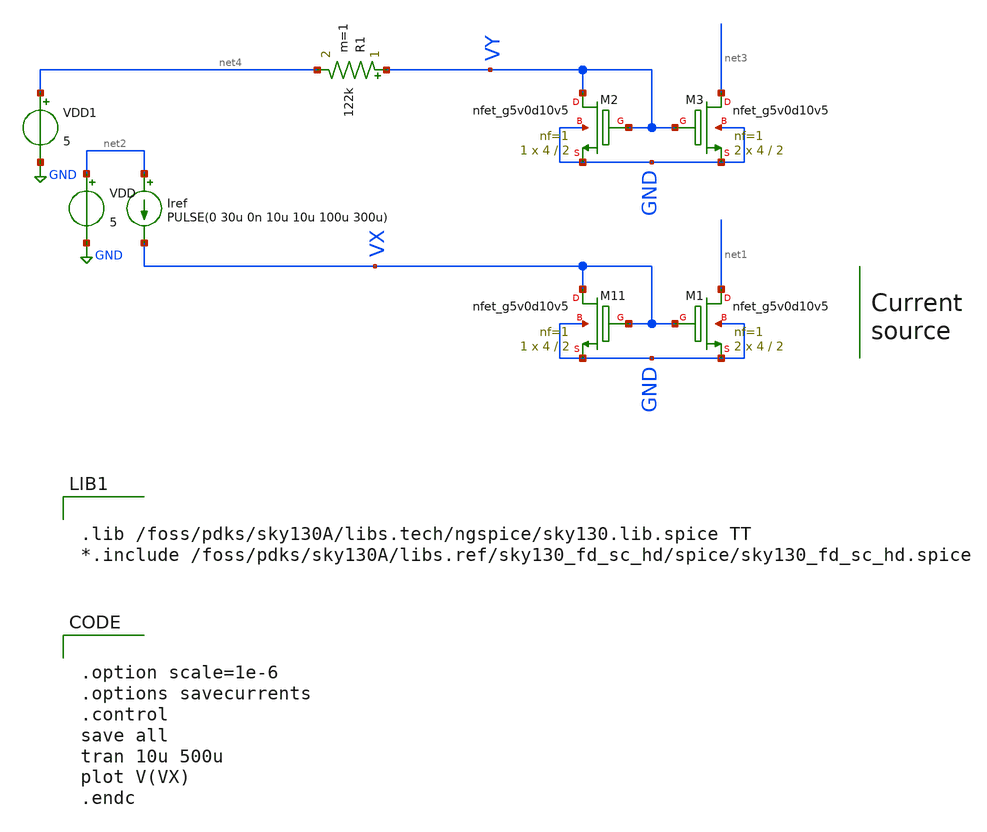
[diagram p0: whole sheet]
** sch_path: xschem/test/tb_current_source.sch
**.subckt tb_current_source
Iref net2 VX PULSE(0 30u 0n 10u 10u 100u 300u)
XM11 VX VX GND GND sky130_fd_pr__nfet_g5v0d10v5 L=2 W=4 nf=1 ad='int((nf+1)/2) * W/nf * 0.29' as='int((nf+2)/2) * W/nf * 0.29'
+ pd='2*int((nf+1)/2) * (W/nf + 0.29)' ps='2*int((nf+2)/2) * (W/nf + 0.29)' nrd='0.29 / W' nrs='0.29 / W'
+ sa=0 sb=0 sd=0 mult=1 m=1
XM1 net1 VX GND GND sky130_fd_pr__nfet_g5v0d10v5 L=2 W=4 nf=1 ad='int((nf+1)/2) * W/nf * 0.29' as='int((nf+2)/2) * W/nf * 0.29'
+ pd='2*int((nf+1)/2) * (W/nf + 0.29)' ps='2*int((nf+2)/2) * (W/nf + 0.29)' nrd='0.29 / W' nrs='0.29 / W'
+ sa=0 sb=0 sd=0 mult=2 m=2
VDD net2 GND 5
XM2 VY VY GND GND sky130_fd_pr__nfet_g5v0d10v5 L=2 W=4 nf=1 ad='int((nf+1)/2) * W/nf * 0.29' as='int((nf+2)/2) * W/nf * 0.29'
+ pd='2*int((nf+1)/2) * (W/nf + 0.29)' ps='2*int((nf+2)/2) * (W/nf + 0.29)' nrd='0.29 / W' nrs='0.29 / W'
+ sa=0 sb=0 sd=0 mult=1 m=1
XM3 net3 VY GND GND sky130_fd_pr__nfet_g5v0d10v5 L=2 W=4 nf=1 ad='int((nf+1)/2) * W/nf * 0.29' as='int((nf+2)/2) * W/nf * 0.29'
+ pd='2*int((nf+1)/2) * (W/nf + 0.29)' ps='2*int((nf+2)/2) * (W/nf + 0.29)' nrd='0.29 / W' nrs='0.29 / W'
+ sa=0 sb=0 sd=0 mult=2 m=2
R1 VY net4 122k m=1
VDD1 net4 GND 5
**** begin user architecture code


.lib /foss/pdks/sky130A/libs.tech/ngspice/sky130.lib.spice TT
*.include /foss/pdks/sky130A/libs.ref/sky130_fd_sc_hd/spice/sky130_fd_sc_hd.spice




.option scale=1e-6
.options savecurrents
.control
save all
tran 10u 500u
plot V(VX)
.endc


**** end user architecture code
**.ends
.GLOBAL GND
.end
